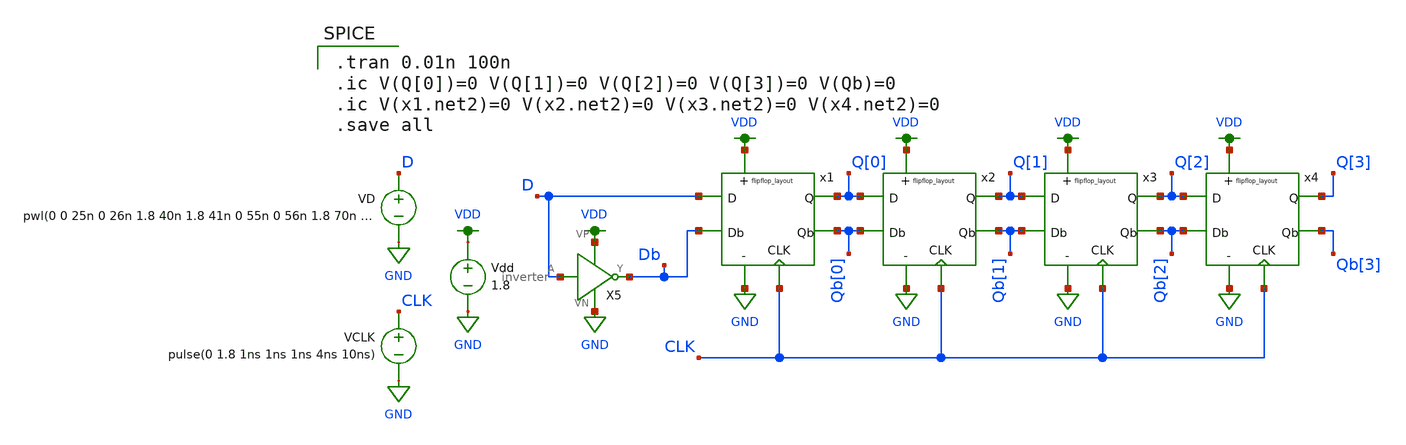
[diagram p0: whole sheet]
** sch_path: mp2/shiftreg_tran.sch
**.subckt shiftreg_tran
X5 D Db VDD GND inverter
Vdd VDD GND 1.8
VCLK CLK GND pulse(0 1.8 1ns 1ns 1ns 4ns 10ns)
VD D GND pwl(0 0 25n 0 26n 1.8 40n 1.8 41n 0 55n 0 56n 1.8 70n 1.8 71n 0)
x1 D Q[0] Db Qb[0] CLK VDD GND flipflop_layout
x2 Q[0] Q[1] Qb[0] Qb[1] CLK VDD GND flipflop_layout
x3 Q[1] Q[2] Qb[1] Qb[2] CLK VDD GND flipflop_layout
x4 Q[2] Q[3] Qb[2] Qb[3] CLK VDD GND flipflop_layout
**** begin user architecture code

.tran 0.01n 100n
.ic V(Q[0])=0 V(Q[1])=0 V(Q[2])=0 V(Q[3])=0 V(Qb)=0
.ic V(x1.net2)=0 V(x2.net2)=0 V(x3.net2)=0 V(x4.net2)=0
.save all


.option wnflag=1
.lib ~/skywater/skywater-pdk/libraries/sky130_fd_pr_ngspice/latest/models/sky130.lib.spice tt

**** end user architecture code
**.ends

* expanding   symbol:  /home/jacob/documents/madvlsi/madvlsi-fa23/mp2/inverter.sym # of pins=4
** sym_path: mp2/inverter.sym
** sch_path: mp2/inverter.sch
.subckt inverter A Y VP VN
*.ipin A
*.opin Y
*.iopin VP
*.iopin VN
XM2 Y A VN VN sky130_fd_pr__nfet_01v8 L=0.15 W=1 nf=1 ad='int((nf+1)/2) * W/nf * 0.29' as='int((nf+2)/2) * W/nf * 0.29'
+ pd='2*int((nf+1)/2) * (W/nf + 0.29)' ps='2*int((nf+2)/2) * (W/nf + 0.29)' nrd='0.29 / W' nrs='0.29 / W'
+ sa=0 sb=0 sd=0 mult=1 m=1
XM1 Y A VP VP sky130_fd_pr__pfet_01v8 L=0.15 W=1 nf=1 ad='int((nf+1)/2) * W/nf * 0.29' as='int((nf+2)/2) * W/nf * 0.29'
+ pd='2*int((nf+1)/2) * (W/nf + 0.29)' ps='2*int((nf+2)/2) * (W/nf + 0.29)' nrd='0.29 / W' nrs='0.29 / W'
+ sa=0 sb=0 sd=0 mult=1 m=1
.ends


* expanding   symbol:  /home/jacob/madvlsi-fa23/mp2/flipflop_layout.sym # of pins=7
** sym_path: mp2/flipflop_layout.sym
** sch_path: mp2/flipflop_layout.sch
.subckt flipflop_layout D Q Db Qb CLK VP VN
*.ipin D
*.ipin Db
*.ipin CLK
*.opin Q
*.opin Qb
*.iopin VP
*.iopin VN
XM1 net2 CLK D VDD sky130_fd_pr__pfet_01v8 L=0.15 W=1 nf=1 ad='int((nf+1)/2) * W/nf * 0.29' as='int((nf+2)/2) * W/nf * 0.29'
+ pd='2*int((nf+1)/2) * (W/nf + 0.29)' ps='2*int((nf+2)/2) * (W/nf + 0.29)' nrd='0.29 / W' nrs='0.29 / W'
+ sa=0 sb=0 sd=0 mult=1 m=1
XM2 net3 CLK Db VDD sky130_fd_pr__pfet_01v8 L=0.15 W=1 nf=1 ad='int((nf+1)/2) * W/nf * 0.29' as='int((nf+2)/2) * W/nf * 0.29'
+ pd='2*int((nf+1)/2) * (W/nf + 0.29)' ps='2*int((nf+2)/2) * (W/nf + 0.29)' nrd='0.29 / W' nrs='0.29 / W'
+ sa=0 sb=0 sd=0 mult=1 m=1
XM3 net2 CLK Q GND sky130_fd_pr__nfet_01v8 L=0.15 W=1 nf=1 ad='int((nf+1)/2) * W/nf * 0.29' as='int((nf+2)/2) * W/nf * 0.29'
+ pd='2*int((nf+1)/2) * (W/nf + 0.29)' ps='2*int((nf+2)/2) * (W/nf + 0.29)' nrd='0.29 / W' nrs='0.29 / W'
+ sa=0 sb=0 sd=0 mult=1 m=1
XM4 net3 CLK Qb GND sky130_fd_pr__nfet_01v8 L=0.15 W=1 nf=1 ad='int((nf+1)/2) * W/nf * 0.29' as='int((nf+2)/2) * W/nf * 0.29'
+ pd='2*int((nf+1)/2) * (W/nf + 0.29)' ps='2*int((nf+2)/2) * (W/nf + 0.29)' nrd='0.29 / W' nrs='0.29 / W'
+ sa=0 sb=0 sd=0 mult=1 m=1
XM5 VN CLK net1 GND sky130_fd_pr__nfet_01v8 L=0.15 W=3.85 nf=1 ad='int((nf+1)/2) * W/nf * 0.29' as='int((nf+2)/2) * W/nf * 0.29'
+ pd='2*int((nf+1)/2) * (W/nf + 0.29)' ps='2*int((nf+2)/2) * (W/nf + 0.29)' nrd='0.29 / W' nrs='0.29 / W'
+ sa=0 sb=0 sd=0 mult=1 m=1
XM6 net1 net2 net3 GND sky130_fd_pr__nfet_01v8 L=0.15 W=1 nf=1 ad='int((nf+1)/2) * W/nf * 0.29' as='int((nf+2)/2) * W/nf * 0.29'
+ pd='2*int((nf+1)/2) * (W/nf + 0.29)' ps='2*int((nf+2)/2) * (W/nf + 0.29)' nrd='0.29 / W' nrs='0.29 / W'
+ sa=0 sb=0 sd=0 mult=1 m=1
XM7 net1 net3 net2 GND sky130_fd_pr__nfet_01v8 L=0.15 W=1 nf=1 ad='int((nf+1)/2) * W/nf * 0.29' as='int((nf+2)/2) * W/nf * 0.29'
+ pd='2*int((nf+1)/2) * (W/nf + 0.29)' ps='2*int((nf+2)/2) * (W/nf + 0.29)' nrd='0.29 / W' nrs='0.29 / W'
+ sa=0 sb=0 sd=0 mult=1 m=1
XM8 VP net2 net3 VDD sky130_fd_pr__pfet_01v8 L=0.15 W=1 nf=1 ad='int((nf+1)/2) * W/nf * 0.29' as='int((nf+2)/2) * W/nf * 0.29'
+ pd='2*int((nf+1)/2) * (W/nf + 0.29)' ps='2*int((nf+2)/2) * (W/nf + 0.29)' nrd='0.29 / W' nrs='0.29 / W'
+ sa=0 sb=0 sd=0 mult=1 m=1
XM9 VP net3 net2 VDD sky130_fd_pr__pfet_01v8 L=0.15 W=1 nf=1 ad='int((nf+1)/2) * W/nf * 0.29' as='int((nf+2)/2) * W/nf * 0.29'
+ pd='2*int((nf+1)/2) * (W/nf + 0.29)' ps='2*int((nf+2)/2) * (W/nf + 0.29)' nrd='0.29 / W' nrs='0.29 / W'
+ sa=0 sb=0 sd=0 mult=1 m=1
XM10 net4 CLK VP VDD sky130_fd_pr__pfet_01v8 L=0.15 W=3.85 nf=1 ad='int((nf+1)/2) * W/nf * 0.29' as='int((nf+2)/2) * W/nf * 0.29'
+ pd='2*int((nf+1)/2) * (W/nf + 0.29)' ps='2*int((nf+2)/2) * (W/nf + 0.29)' nrd='0.29 / W' nrs='0.29 / W'
+ sa=0 sb=0 sd=0 mult=1 m=1
XM11 Qb Q net4 VDD sky130_fd_pr__pfet_01v8 L=0.15 W=1 nf=1 ad='int((nf+1)/2) * W/nf * 0.29' as='int((nf+2)/2) * W/nf * 0.29'
+ pd='2*int((nf+1)/2) * (W/nf + 0.29)' ps='2*int((nf+2)/2) * (W/nf + 0.29)' nrd='0.29 / W' nrs='0.29 / W'
+ sa=0 sb=0 sd=0 mult=1 m=1
XM12 Q Qb net4 VDD sky130_fd_pr__pfet_01v8 L=0.15 W=1 nf=1 ad='int((nf+1)/2) * W/nf * 0.29' as='int((nf+2)/2) * W/nf * 0.29'
+ pd='2*int((nf+1)/2) * (W/nf + 0.29)' ps='2*int((nf+2)/2) * (W/nf + 0.29)' nrd='0.29 / W' nrs='0.29 / W'
+ sa=0 sb=0 sd=0 mult=1 m=1
XM13 VN Q Qb GND sky130_fd_pr__nfet_01v8 L=0.15 W=1 nf=1 ad='int((nf+1)/2) * W/nf * 0.29' as='int((nf+2)/2) * W/nf * 0.29'
+ pd='2*int((nf+1)/2) * (W/nf + 0.29)' ps='2*int((nf+2)/2) * (W/nf + 0.29)' nrd='0.29 / W' nrs='0.29 / W'
+ sa=0 sb=0 sd=0 mult=1 m=1
XM14 VN Qb Q GND sky130_fd_pr__nfet_01v8 L=0.15 W=1 nf=1 ad='int((nf+1)/2) * W/nf * 0.29' as='int((nf+2)/2) * W/nf * 0.29'
+ pd='2*int((nf+1)/2) * (W/nf + 0.29)' ps='2*int((nf+2)/2) * (W/nf + 0.29)' nrd='0.29 / W' nrs='0.29 / W'
+ sa=0 sb=0 sd=0 mult=1 m=1
.ends

.GLOBAL VDD
.GLOBAL GND
.end
